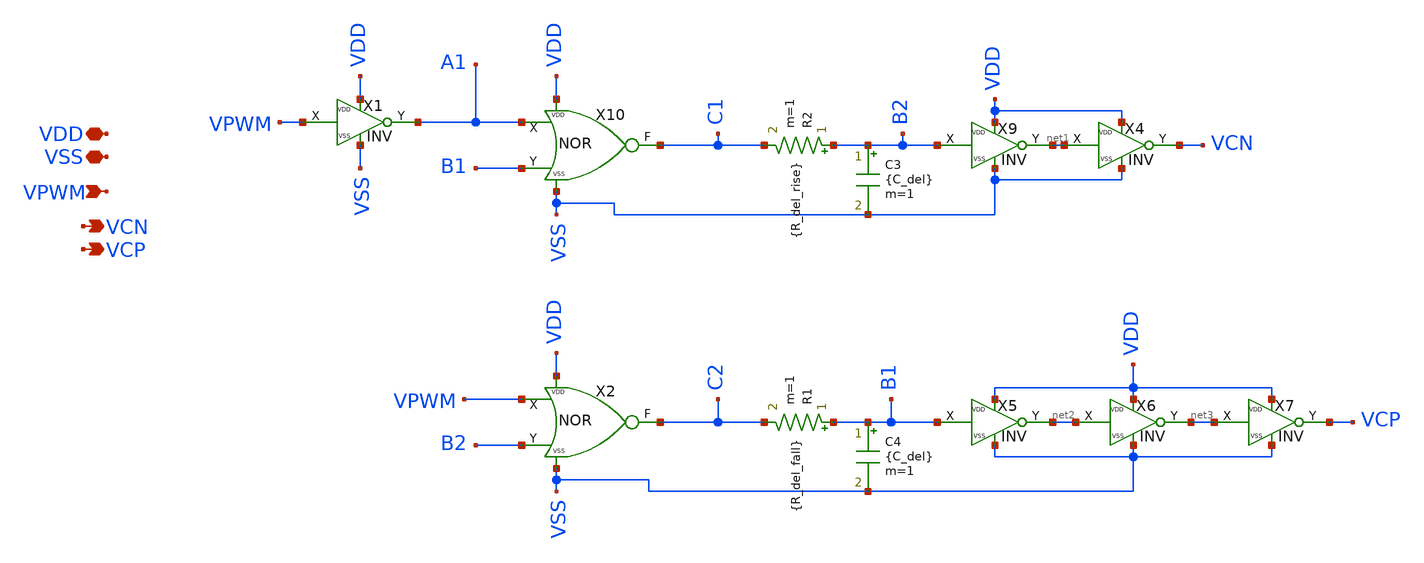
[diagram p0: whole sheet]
** sch_path: xschem/NOL/NOL.sch
**.subckt NOL VDD VPWM VCN VSS VCP
*.iopin VDD
*.ipin VPWM
*.opin VCN
*.iopin VSS
*.opin VCP
C3 B2 VSS {C_del} m=1
R1 B1 C2 {R_del_fall} m=1
C4 B1 VSS {C_del} m=1
R2 B2 C1 {R_del_rise} m=1
X9 B2 net1 VDD VSS INV
X10 VDD VSS C1 A1 B1 NOR
X4 net1 VCN VDD VSS INV
X5 B1 net2 VDD VSS INV
X6 net2 net3 VDD VSS INV
X7 net3 VCP VDD VSS INV
X1 VPWM A1 VDD VSS INV
X2 VDD VSS C2 VPWM B2 NOR
**** begin user architecture code



**** end user architecture code
**.ends

* expanding   symbol:  ../DigitalGates/INV.sym # of pins=4
** sym_path: xschem/DigitalGates/INV.sym
** sch_path: xschem/DigitalGates/INV.sch
.subckt INV X Y VDD VSS
*.iopin VDD
*.ipin X
*.opin Y
*.iopin VSS
XM3 Y X VSS VSS sg13_lv_nmos w={w_inv} l={l_inv} ng=1 m={mult} mm_ok=1
XM4 Y X VDD VDD sg13_lv_pmos w={w_inv} l={l_inv} ng=1 m={mult*3} mm_ok=1
**** begin user architecture code



**** end user architecture code
.ends


* expanding   symbol:  ../DigitalGates/NOR.sym # of pins=5
** sym_path: xschem/DigitalGates/NOR.sym
** sch_path: xschem/DigitalGates/NOR.sch
.subckt NOR VDD VSS F X Y
*.iopin VDD
*.ipin X
*.opin F
*.iopin VSS
*.ipin Y
XM1 F Y VSS VSS sg13_lv_nmos w={w_N_NOR} l={l_N_NOR} ng=1 m={mult} mm_ok=1
XM2 net1 X VDD VDD sg13_lv_pmos w={w_P_NOR} l={l_P_NOR} ng=1 m={mult*3} mm_ok=1
XM4 F Y net1 VDD sg13_lv_pmos w={w_P_NOR} l={l_P_NOR} ng=1 m={mult*3} mm_ok=1
XM3 F X VSS VSS sg13_lv_nmos w={w_N_NOR} l={l_N_NOR} ng=1 m={mult} mm_ok=1
**** begin user architecture code



**** end user architecture code
.ends

.end
